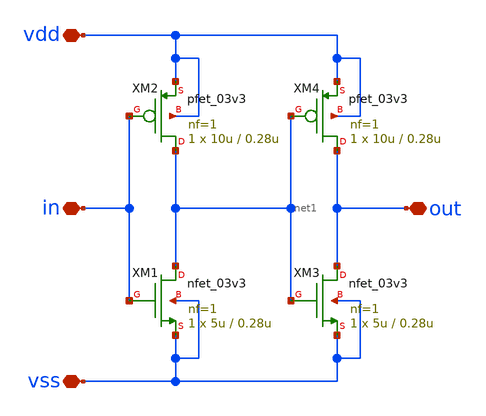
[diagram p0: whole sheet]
** sch_path: designs/libs/qw_core_analog_pkedit/delay.sch
**.subckt delay vdd vss in out
*.iopin vdd
*.iopin vss
*.iopin in
*.iopin out
XM1 net1 in vss vss nfet_03v3 L=0.28u W=5u nf=1 ad='int((nf+1)/2) * W/nf * 0.18u' as='int((nf+2)/2) * W/nf * 0.18u'
+ pd='2*int((nf+1)/2) * (W/nf + 0.18u)' ps='2*int((nf+2)/2) * (W/nf + 0.18u)' nrd='0.18u / W' nrs='0.18u / W'
+ sa=0 sb=0 sd=0 m=1
XM2 net1 in vdd vdd pfet_03v3 L=0.28u W=10u nf=1 ad='int((nf+1)/2) * W/nf * 0.18u' as='int((nf+2)/2) * W/nf * 0.18u'
+ pd='2*int((nf+1)/2) * (W/nf + 0.18u)' ps='2*int((nf+2)/2) * (W/nf + 0.18u)' nrd='0.18u / W' nrs='0.18u / W'
+ sa=0 sb=0 sd=0 m=1
XM3 out net1 vss vss nfet_03v3 L=0.28u W=5u nf=1 ad='int((nf+1)/2) * W/nf * 0.18u' as='int((nf+2)/2) * W/nf * 0.18u'
+ pd='2*int((nf+1)/2) * (W/nf + 0.18u)' ps='2*int((nf+2)/2) * (W/nf + 0.18u)' nrd='0.18u / W' nrs='0.18u / W'
+ sa=0 sb=0 sd=0 m=1
XM4 out net1 vdd vdd pfet_03v3 L=0.28u W=10u nf=1 ad='int((nf+1)/2) * W/nf * 0.18u' as='int((nf+2)/2) * W/nf * 0.18u'
+ pd='2*int((nf+1)/2) * (W/nf + 0.18u)' ps='2*int((nf+2)/2) * (W/nf + 0.18u)' nrd='0.18u / W' nrs='0.18u / W'
+ sa=0 sb=0 sd=0 m=1
**.ends
.end
